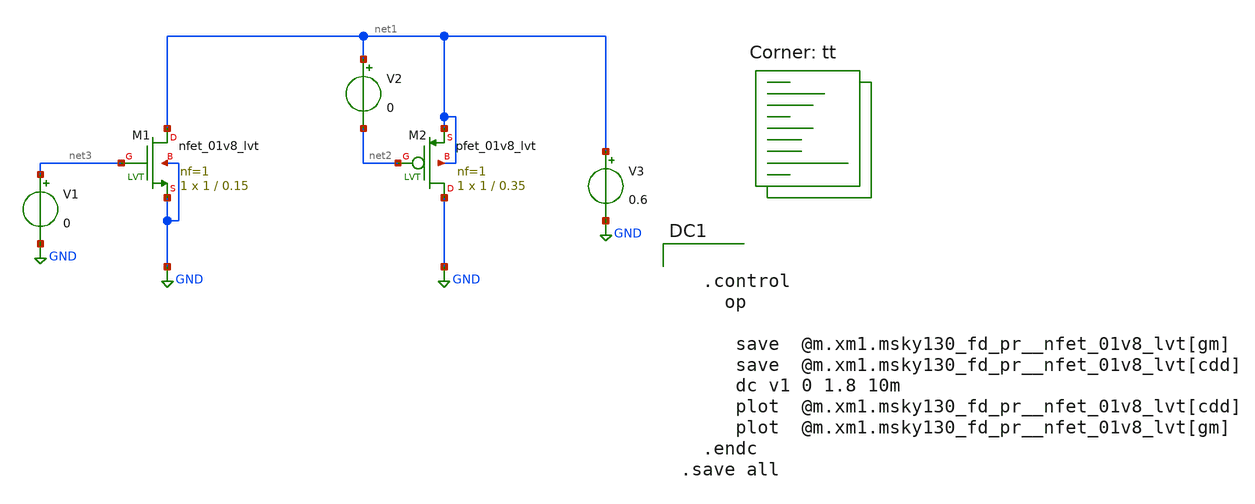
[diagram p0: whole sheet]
** sch_path: pll/lc_vco_lib/Hossam_Tarek/lc_osc_complementary_pmos_tb/xschem/MOS_char.sch
**.subckt MOS_char
XM1 net1 net3 GND GND sky130_fd_pr__nfet_01v8_lvt L=0.15 W=1 nf=1 ad='int((nf+1)/2) * W/nf * 0.29' as='int((nf+2)/2) * W/nf * 0.29'
+ pd='2*int((nf+1)/2) * (W/nf + 0.29)' ps='2*int((nf+2)/2) * (W/nf + 0.29)' nrd='0.29 / W' nrs='0.29 / W'
+ sa=0 sb=0 sd=0 mult=1 m=1
XM2 GND net2 net1 net1 sky130_fd_pr__pfet_01v8_lvt L=0.35 W=1 nf=1 ad='int((nf+1)/2) * W/nf * 0.29' as='int((nf+2)/2) * W/nf * 0.29'
+ pd='2*int((nf+1)/2) * (W/nf + 0.29)' ps='2*int((nf+2)/2) * (W/nf + 0.29)' nrd='0.29 / W' nrs='0.29 / W'
+ sa=0 sb=0 sd=0 mult=1 m=1
V1 net3 GND 0
V2 net1 net2 0
V3 net1 GND 0.6
**** begin user architecture code


  .control
    op

     save  @m.xm1.msky130_fd_pr__nfet_01v8_lvt[gm]
     save  @m.xm1.msky130_fd_pr__nfet_01v8_lvt[cdd]
     dc v1 0 1.8 10m
     plot  @m.xm1.msky130_fd_pr__nfet_01v8_lvt[cdd]
     plot  @m.xm1.msky130_fd_pr__nfet_01v8_lvt[gm]
  .endc
.save all

.lib $::SKYWATER_MODELS/sky130.lib.spice tt
**** end user architecture code
**.ends
.GLOBAL GND
.end
